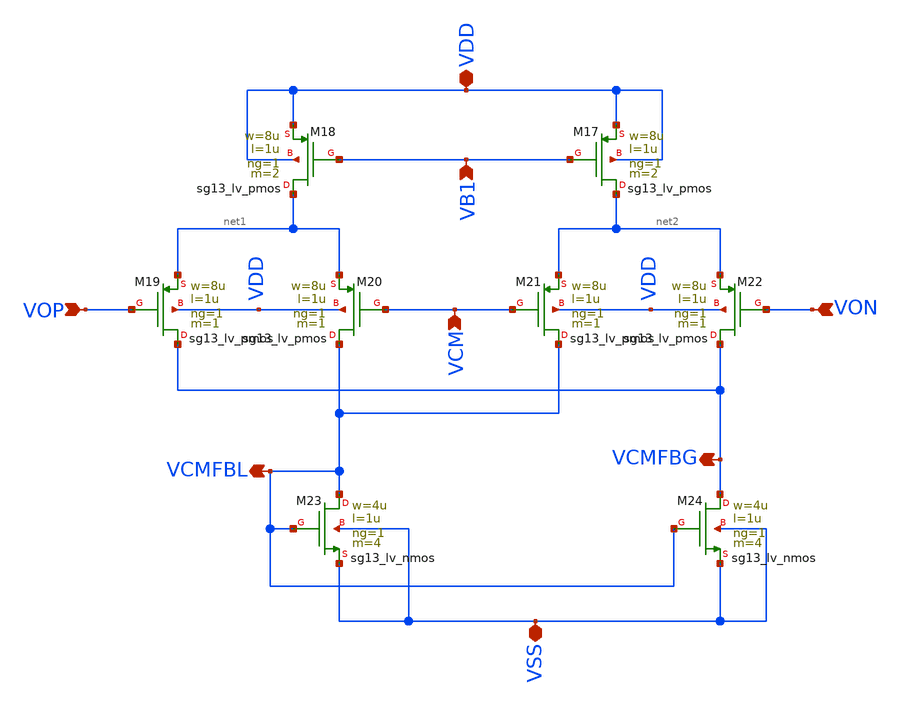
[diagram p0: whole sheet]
** sch_path: BTDay8-Ex/AMP_CMFB_INV_08V.sch
**.subckt AMP_CMFB_INV_08V VCM VCMFBL VCMFBG VOP VB1 VSS VDD VON
*.ipin VCM
*.opin VCMFBL
*.opin VCMFBG
*.ipin VOP
*.ipin VB1
*.iopin VSS
*.iopin VDD
*.ipin VON
XM17 net2 VB1 VDD VDD sg13_lv_pmos w=8u l=1u ng=1 m=2 mm_ok=1
XM18 net1 VB1 VDD VDD sg13_lv_pmos w=8u l=1u ng=1 m=2 mm_ok=1
XM19 VCMFBG VOP net1 VDD sg13_lv_pmos w=8u l=1u ng=1 m=1 mm_ok=1
XM20 VCMFBL VCM net1 VDD sg13_lv_pmos w=8u l=1u ng=1 m=1 mm_ok=1
XM21 VCMFBL VCM net2 VDD sg13_lv_pmos w=8u l=1u ng=1 m=1 mm_ok=1
XM22 VCMFBG VON net2 VDD sg13_lv_pmos w=8u l=1u ng=1 m=1 mm_ok=1
XM23 VCMFBL VCMFBL VSS VSS sg13_lv_nmos w=4u l=1u ng=1 m=4 mm_ok=1
XM24 VCMFBG VCMFBL VSS VSS sg13_lv_nmos w=4u l=1u ng=1 m=4 mm_ok=1
**.ends
.end
